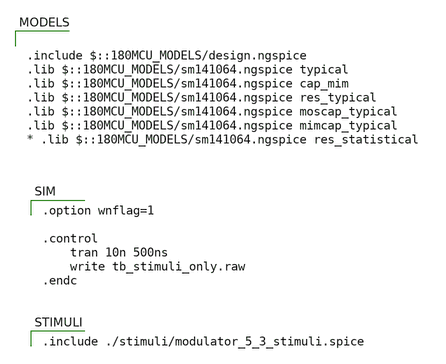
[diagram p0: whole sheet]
** sch_path: xschem/tb_stimuli_only.sch
**.subckt tb_stimuli_only
**** begin user architecture code

.option wnflag=1

.control
    tran 10n 500ns
    write tb_stimuli_only.raw
.endc



.include ./stimuli/modulator_5_3_stimuli.spice


.include $::180MCU_MODELS/design.ngspice
.lib $::180MCU_MODELS/sm141064.ngspice typical
.lib $::180MCU_MODELS/sm141064.ngspice cap_mim
.lib $::180MCU_MODELS/sm141064.ngspice res_typical
.lib $::180MCU_MODELS/sm141064.ngspice moscap_typical
.lib $::180MCU_MODELS/sm141064.ngspice mimcap_typical
* .lib $::180MCU_MODELS/sm141064.ngspice res_statistical

**** end user architecture code
**.ends
.end
